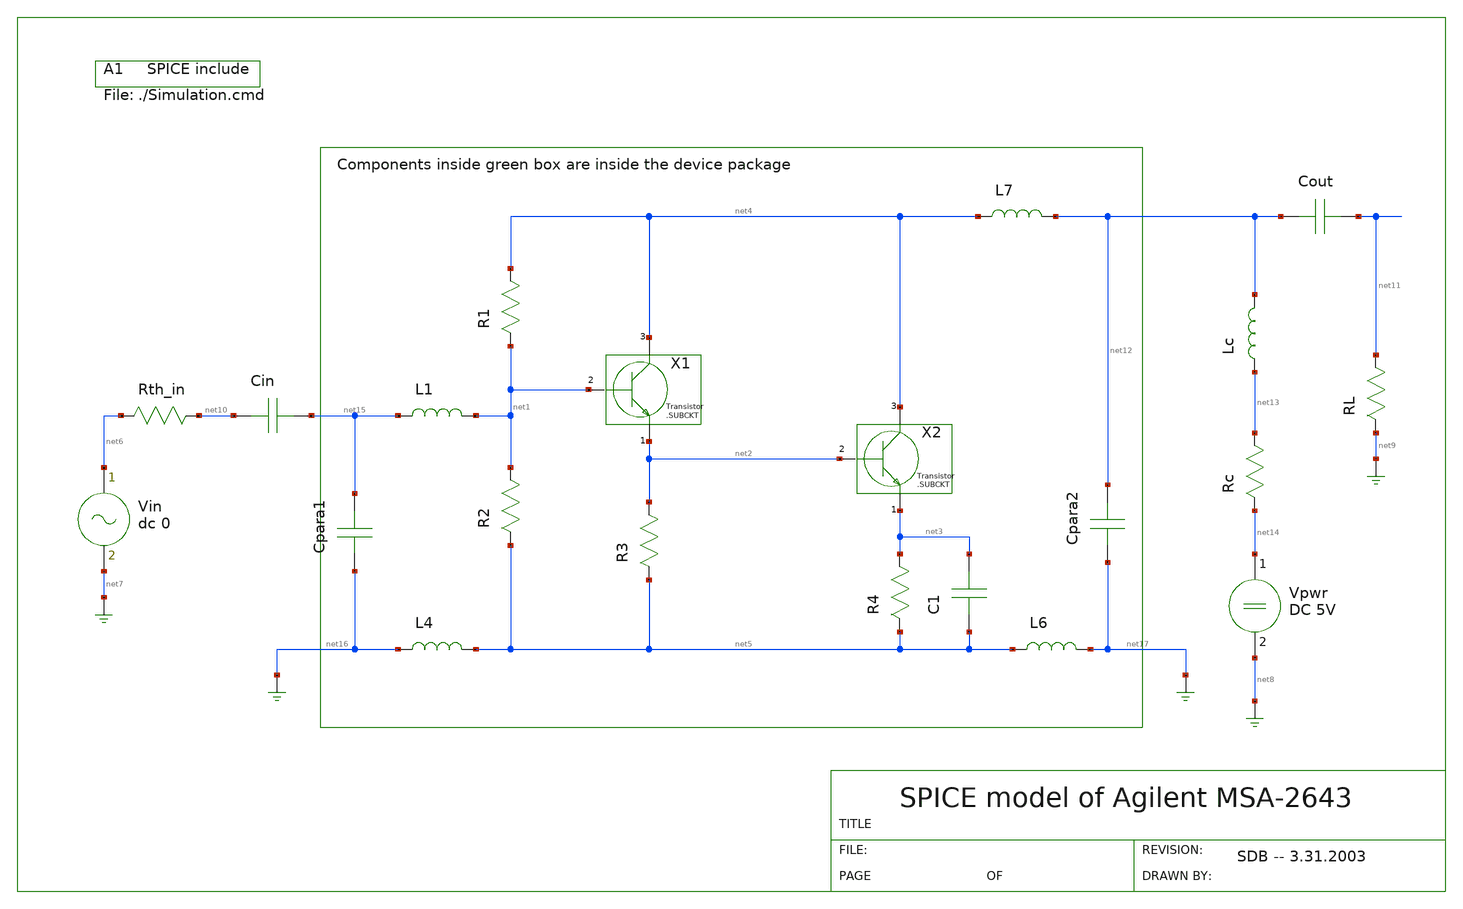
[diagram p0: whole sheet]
** sch_path: xschem_library/gschem_import/MSA-2643.sch
**.subckt MSA-2643
R1 net4 net1 560
R2 net1 net5 660
R3 net2 net5 250
R4 net3 net5 5
X1 net4 net2 net1
X2 net4 net3 net2
C1 net5 net3 4pF
Vpwr net14 net8 DC 5V
Vin net6 net7 dc 0
Rth_in net10 net6 50
RL net11 net9 50
Lc net12 net13 22nH
Rc net13 net14 50
Cout net12 net11 47pF
Cin net10 net15 47pF
A1
L4 net5 net16 0.386nH
L6 net17 net5 0.313nH
L1 net1 net15 0.833nH
L7 net12 net4 0.407nH
Cpara1 net16 net15 0.158pF
Cpara2 net17 net12 0.155pF
**.ends
.end
